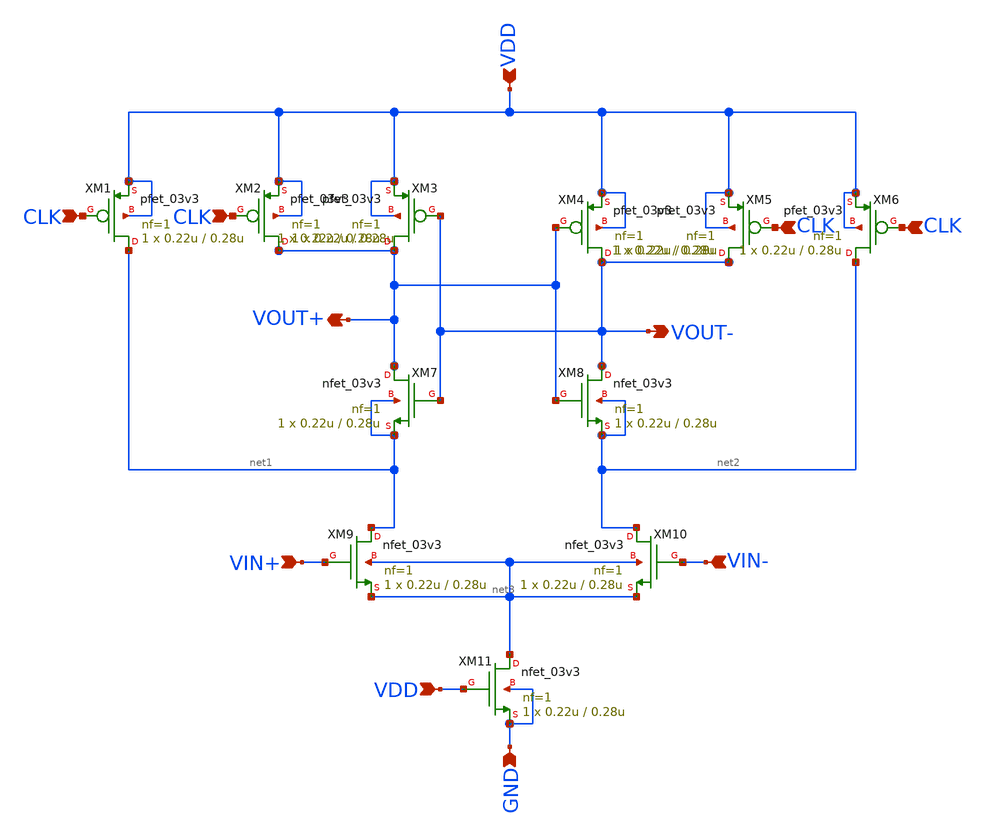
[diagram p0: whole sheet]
** sch_path: SAR_ADC/xschem/spice/symbols/strong_arm.sch
**.subckt strong_arm CLK CLK CLK CLK VDD VIN+ VIN- VDD GND VOUT+ VOUT-
*.ipin CLK
*.ipin CLK
*.ipin CLK
*.ipin CLK
*.ipin VDD
*.ipin VIN+
*.ipin VIN-
*.ipin VDD
*.ipin GND
*.opin VOUT+
*.opin VOUT-
XM1 net1 CLK VDD VDD pfet_03v3 L=0.28u W=0.22u nf=1 ad='int((nf+1)/2) * W/nf * 0.18u' as='int((nf+2)/2) * W/nf * 0.18u'
+ pd='2*int((nf+1)/2) * (W/nf + 0.18u)' ps='2*int((nf+2)/2) * (W/nf + 0.18u)' nrd='0.18u / W' nrs='0.18u / W'
+ sa=0 sb=0 sd=0 m=1
XM2 VOUT+ CLK VDD VDD pfet_03v3 L=0.28u W=0.22u nf=1 ad='int((nf+1)/2) * W/nf * 0.18u' as='int((nf+2)/2) * W/nf * 0.18u'
+ pd='2*int((nf+1)/2) * (W/nf + 0.18u)' ps='2*int((nf+2)/2) * (W/nf + 0.18u)' nrd='0.18u / W' nrs='0.18u / W'
+ sa=0 sb=0 sd=0 m=1
XM3 VOUT+ VOUT- VDD VDD pfet_03v3 L=0.28u W=0.22u nf=1 ad='int((nf+1)/2) * W/nf * 0.18u' as='int((nf+2)/2) * W/nf * 0.18u'
+ pd='2*int((nf+1)/2) * (W/nf + 0.18u)' ps='2*int((nf+2)/2) * (W/nf + 0.18u)' nrd='0.18u / W' nrs='0.18u / W'
+ sa=0 sb=0 sd=0 m=1
XM4 VOUT- VOUT+ VDD VDD pfet_03v3 L=0.28u W=0.22u nf=1 ad='int((nf+1)/2) * W/nf * 0.18u' as='int((nf+2)/2) * W/nf * 0.18u'
+ pd='2*int((nf+1)/2) * (W/nf + 0.18u)' ps='2*int((nf+2)/2) * (W/nf + 0.18u)' nrd='0.18u / W' nrs='0.18u / W'
+ sa=0 sb=0 sd=0 m=1
XM5 VOUT- CLK VDD VDD pfet_03v3 L=0.28u W=0.22u nf=1 ad='int((nf+1)/2) * W/nf * 0.18u' as='int((nf+2)/2) * W/nf * 0.18u'
+ pd='2*int((nf+1)/2) * (W/nf + 0.18u)' ps='2*int((nf+2)/2) * (W/nf + 0.18u)' nrd='0.18u / W' nrs='0.18u / W'
+ sa=0 sb=0 sd=0 m=1
XM6 net2 CLK VDD VDD pfet_03v3 L=0.28u W=0.22u nf=1 ad='int((nf+1)/2) * W/nf * 0.18u' as='int((nf+2)/2) * W/nf * 0.18u'
+ pd='2*int((nf+1)/2) * (W/nf + 0.18u)' ps='2*int((nf+2)/2) * (W/nf + 0.18u)' nrd='0.18u / W' nrs='0.18u / W'
+ sa=0 sb=0 sd=0 m=1
XM7 VOUT+ VOUT- net1 net1 nfet_03v3 L=0.28u W=0.22u nf=1 ad='int((nf+1)/2) * W/nf * 0.18u' as='int((nf+2)/2) * W/nf * 0.18u'
+ pd='2*int((nf+1)/2) * (W/nf + 0.18u)' ps='2*int((nf+2)/2) * (W/nf + 0.18u)' nrd='0.18u / W' nrs='0.18u / W'
+ sa=0 sb=0 sd=0 m=1
XM8 VOUT- VOUT+ net2 net2 nfet_03v3 L=0.28u W=0.22u nf=1 ad='int((nf+1)/2) * W/nf * 0.18u' as='int((nf+2)/2) * W/nf * 0.18u'
+ pd='2*int((nf+1)/2) * (W/nf + 0.18u)' ps='2*int((nf+2)/2) * (W/nf + 0.18u)' nrd='0.18u / W' nrs='0.18u / W'
+ sa=0 sb=0 sd=0 m=1
XM9 net1 VIN+ net3 net3 nfet_03v3 L=0.28u W=0.22u nf=1 ad='int((nf+1)/2) * W/nf * 0.18u' as='int((nf+2)/2) * W/nf * 0.18u'
+ pd='2*int((nf+1)/2) * (W/nf + 0.18u)' ps='2*int((nf+2)/2) * (W/nf + 0.18u)' nrd='0.18u / W' nrs='0.18u / W'
+ sa=0 sb=0 sd=0 m=1
XM10 net2 VIN- net3 net3 nfet_03v3 L=0.28u W=0.22u nf=1 ad='int((nf+1)/2) * W/nf * 0.18u' as='int((nf+2)/2) * W/nf * 0.18u'
+ pd='2*int((nf+1)/2) * (W/nf + 0.18u)' ps='2*int((nf+2)/2) * (W/nf + 0.18u)' nrd='0.18u / W' nrs='0.18u / W'
+ sa=0 sb=0 sd=0 m=1
XM11 net3 VDD GND GND nfet_03v3 L=0.28u W=0.22u nf=1 ad='int((nf+1)/2) * W/nf * 0.18u' as='int((nf+2)/2) * W/nf * 0.18u'
+ pd='2*int((nf+1)/2) * (W/nf + 0.18u)' ps='2*int((nf+2)/2) * (W/nf + 0.18u)' nrd='0.18u / W' nrs='0.18u / W'
+ sa=0 sb=0 sd=0 m=1
**.ends
.end
